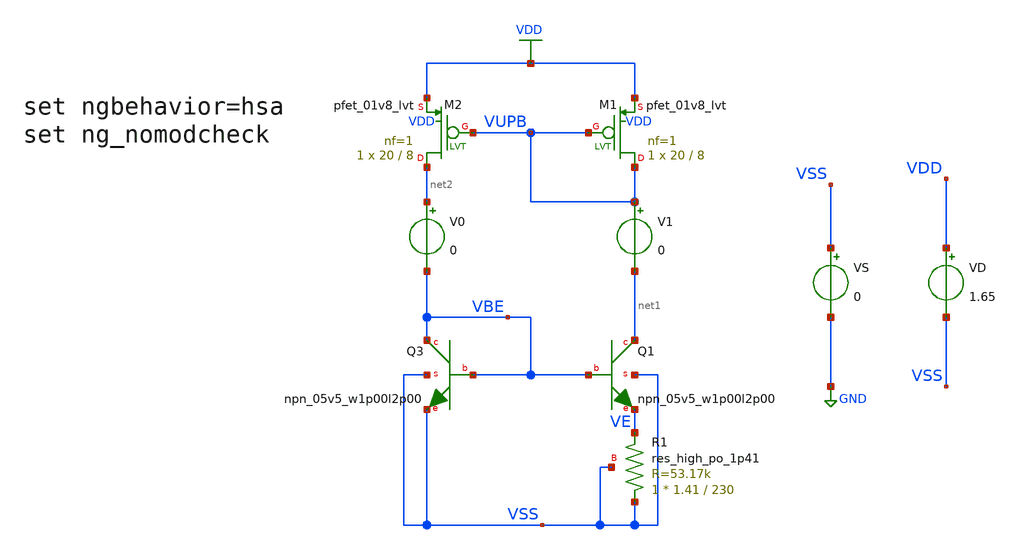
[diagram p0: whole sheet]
** sch_path: designs/temp_char_ptat_ctat.sch
**.subckt temp_char_ptat_ctat
VD VDD VSS 1.65
.save i(vd)
VS VSS GND 0
XM1 VUPB VUPB VDD VDD sky130_fd_pr__pfet_01v8_lvt L=8 W=20 nf=1 ad='int((nf+1)/2) * W/nf * 0.29' as='int((nf+2)/2) * W/nf * 0.29'
+ pd='2*int((nf+1)/2) * (W/nf + 0.29)' ps='2*int((nf+2)/2) * (W/nf + 0.29)' nrd='0.29 / W' nrs='0.29 / W'
+ sa=0 sb=0 sd=0 mult=1 m=1
XM2 net2 VUPB VDD VDD sky130_fd_pr__pfet_01v8_lvt L=8 W=20 nf=1 ad='int((nf+1)/2) * W/nf * 0.29' as='int((nf+2)/2) * W/nf * 0.29'
+ pd='2*int((nf+1)/2) * (W/nf + 0.29)' ps='2*int((nf+2)/2) * (W/nf + 0.29)' nrd='0.29 / W' nrs='0.29 / W'
+ sa=0 sb=0 sd=0 mult=1 m=1
XQ1 net1 VBE VE VSS sky130_fd_pr__npn_05v5_w1p00l2p00
XQ3 VBE VBE VSS VSS sky130_fd_pr__npn_05v5_w1p00l2p00
V0 net2 VBE 0
.save i(v0)
V1 VUPB net1 0
.save i(v1)
XR1 VSS VE VSS sky130_fd_pr__res_high_po_1p41 L=230 mult=1 m=1
**** begin user architecture code


** Analysis Requests **
** Outputs Requests **
.option wnflag=1
.option savecurrents
.control
save all
dc temp -40 125 5
remzerovec
wrdata ~/.xschem/simulations/temp_char_ptat_ctat.txt i(V0) i(V1) v(VBE) v(VUPB)
*plot V(VBE), V(VUPB)
plot V(VE)/I(V1)
*plot I(V0), I(V1)
quit 0
.endc



** opencircuitdesign pdks install
.lib /foss/pdks/sky130A/libs.tech/ngspice/sky130.lib.corners.spice sshh

**** end user architecture code
**.ends
.GLOBAL GND
.GLOBAL VDD
.end
